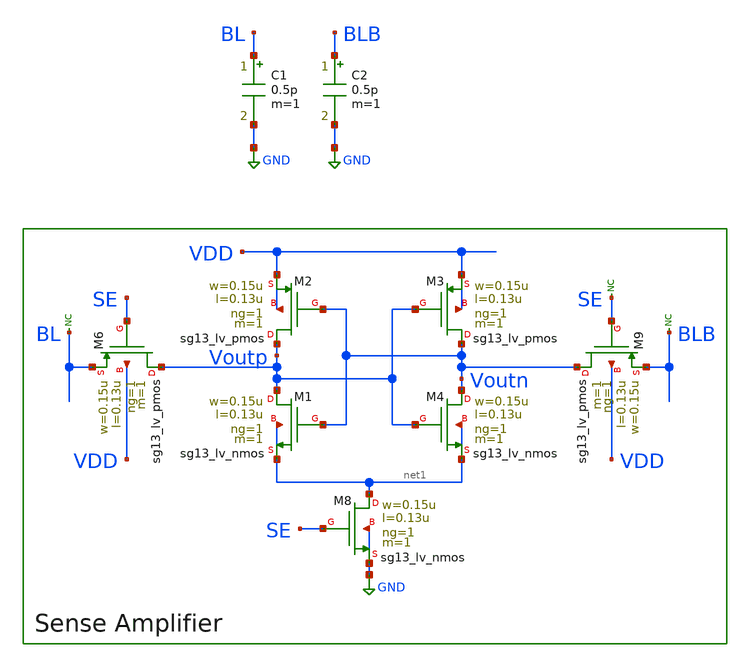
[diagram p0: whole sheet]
** sch_path: xschem/offset_voltage_tester/offset-voltage-tester.sch
**.subckt offset-voltage-tester
XM8 net1 SE GND GND sg13_lv_nmos w=0.15u l=0.13u ng=1 m=1 mm_ok=1
XM1 Voutp Voutn net1 net1 sg13_lv_nmos w=0.15u l=0.13u ng=1 m=1 mm_ok=1
XM3 Voutn Voutp VDD VDD sg13_lv_pmos w=0.15u l=0.13u ng=1 m=1 mm_ok=1
XM2 Voutp Voutn VDD VDD sg13_lv_pmos w=0.15u l=0.13u ng=1 m=1 mm_ok=1
XM4 Voutn Voutp net1 net1 sg13_lv_nmos w=0.15u l=0.13u ng=1 m=1 mm_ok=1
XM6 Voutp SE BL VDD sg13_lv_pmos w=0.15u l=0.13u ng=1 m=1 mm_ok=1
XM9 Voutn SE BLB VDD sg13_lv_pmos w=0.15u l=0.13u ng=1 m=1 mm_ok=1
* noconn SE
* noconn BLB
* noconn BL
C1 BL GND 0.5p m=1
C2 BLB GND 0.5p m=1
**** begin user architecture code



.lib cornerMOSlv.lib mos_tt_mismatch

.param VDD=1.2
.param VCM=1.2
.param vind=0

.param TPER=10n
.param TSE_DLY=4n
.param TSE_W=3n
.param TR=100p
.param TF=100p
.param TEVAL=6.5n

VDD_S VDD 0 {VDD}
VSE SE 0 PULSE(0 {VDD} {TSE_DLY} {TR} {TF} {TSE_W} {TPER})
* SE Pulse:
* 0V -> VDD @ TSE_DLY
* Stays high for TSE_W
* Repeats every TPER

B_BLDRV BLDRV 0 V = {VCM + vind / 2}
B_BLBDRV BLBDRV 0 V = {VCM - vind / 2}

RBL BLDRV BL 50
RBLB BLBDRV BLB 50

.control
set noaskquit
set numdgt=10

let vin_min = -0.005
let vin_max =  0.005
let nbit = 12
let voutd_th = 0

let tstop = 10n
let teval = 6.5n

let vind_range = vin_max - vin_min
let vind_dir = 1
let reset_state = 1
let count = 1
let vind_sar_val = vin_min + vind_range / 2
let vind_val = vin_min
let vos_r = 0
let vos_f = 0
let vod_last = 0
let lsb = 0
let vos_candidate = 0

while 1

  if reset_state = 1
    if vind_dir = 1
      let vind_val = vin_min
    else
      let vind_val = vin_max
    end

    alterparam vind = $&vind_val
    reset
    tran 5p $&tstop
    meas tran vop FIND v(voutp) AT=$&teval
    meas tran von FIND v(voutn) AT=$&teval
    let vod_last = $&vop - $&von

    let reset_state = 0
    continue
  end

  let vind_val = vind_sar_val
  alterparam vind = $&vind_val
  reset
  tran 5p $&tstop
  meas tran vop FIND v(voutp) AT=$&teval
  meas tran von FIND v(voutn) AT=$&teval
  let vod_last = $&vop - $&von

  if count < nbit
    let count = count + 1

    if vod_last > voutd_th
      let vind_sar_val = vind_sar_val - vind_range / (2^count)
      if vind_dir = 1
        let reset_state = 1
      end
    else
      let vind_sar_val = vind_sar_val + vind_range / (2^count)
      if vind_dir = 0
        let reset_state = 1
      end
    end

  else
    let lsb = vind_range / (2^count)

    if vod_last > voutd_th
      let vos_candidate = vind_sar_val - lsb/2
    else
      let vos_candidate = vind_sar_val + lsb/2
    end

    if vind_dir = 1
      let vos_r = $&vos_candidate

      let vind_dir = 0
      let count = 1
      let vind_sar_val = vin_min + vind_range / 2
      let reset_state = 1
      let vind_val = vin_max
      continue
    else
      let vos_f = $&vos_candidate
      break
    end
  end

end

let vos_avg = (vos_r + vos_f) / 2
let vos_diff = vos_r - vos_f

echo 'vos_r = ' $&vos_r
echo 'vos_f = ' $&vos_f
echo 'diff  = ' $&vos_diff
.endc



**** end user architecture code
**.ends
.GLOBAL GND
.end
